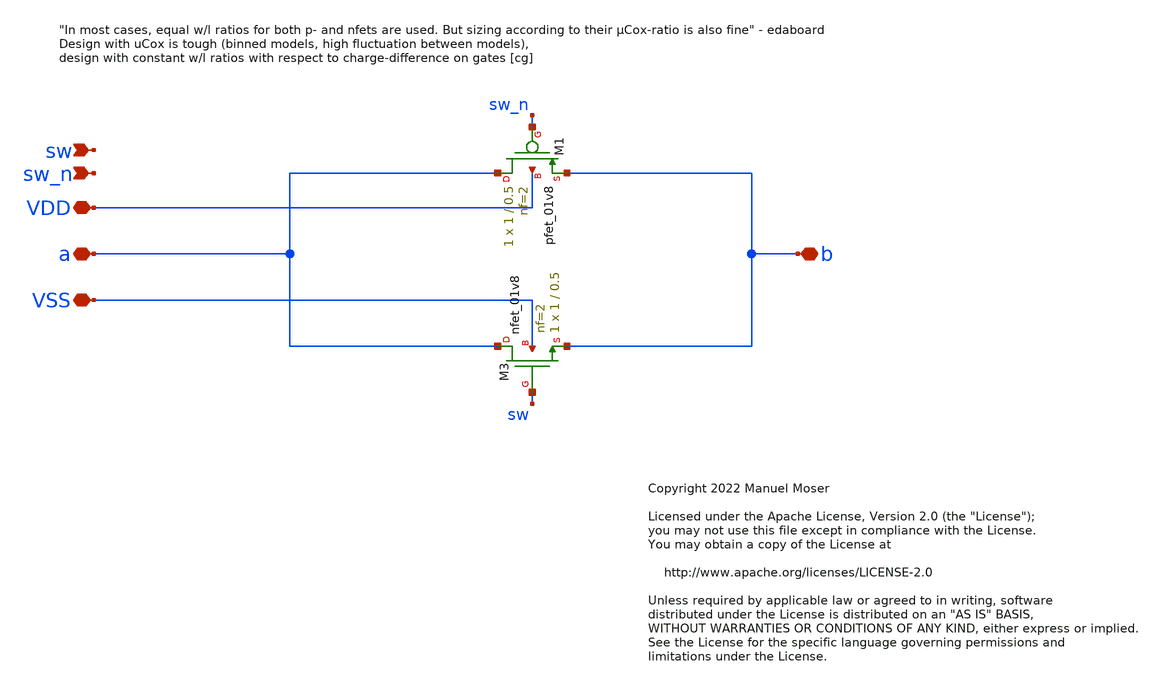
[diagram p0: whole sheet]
** sch_path: hgu/xschem/adc_vcm_switch.sch
* Copyright 2022 Manuel Moser
* Licensed under the Apache License, Version 2.0 (the "License");
**.subckt adc_vcm_switch VSS VDD sw_n sw a b
*.iopin VSS
*.iopin VDD
*.ipin sw_n
*.ipin sw
*.iopin a
*.iopin b
XM1 a sw_n b VDD sky130_fd_pr__pfet_01v8 L=0.5 W=1 nf=2 ad='int((nf+1)/2) * W/nf * 0.29' as='int((nf+2)/2) * W/nf * 0.29'
+ pd='2*int((nf+1)/2) * (W/nf + 0.29)' ps='2*int((nf+2)/2) * (W/nf + 0.29)' nrd='0.29 / W' nrs='0.29 / W'
+ sa=0 sb=0 sd=0 mult=1 m=1
XM3 a sw b VSS sky130_fd_pr__nfet_01v8 L=0.5 W=1 nf=2 ad='int((nf+1)/2) * W/nf * 0.29' as='int((nf+2)/2) * W/nf * 0.29'
+ pd='2*int((nf+1)/2) * (W/nf + 0.29)' ps='2*int((nf+2)/2) * (W/nf + 0.29)' nrd='0.29 / W' nrs='0.29 / W'
+ sa=0 sb=0 sd=0 mult=1 m=1
**.ends
.end
